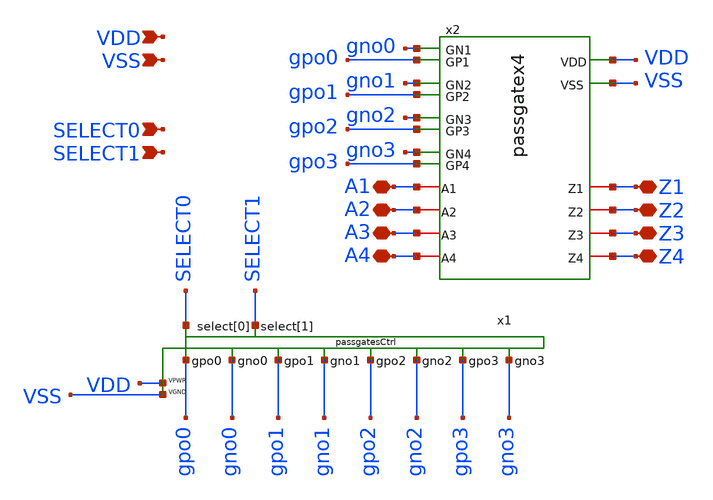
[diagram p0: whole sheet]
** sch_path: xschem/mux4onehot.sch
**.subckt mux4onehot VSS VDD A1 A2 A3 A4 Z1 Z2 Z3 Z4 SELECT0 SELECT1
*.ipin VSS
*.ipin VDD
*.iopin A1
*.iopin A2
*.iopin A3
*.iopin A4
*.iopin Z1
*.iopin Z2
*.iopin Z3
*.iopin Z4
*.ipin SELECT0
*.ipin SELECT1
x1 VSS VDD gno0 gno1 gno2 gno3 gpo0 gpo1 gpo2 gpo3 SELECT0 SELECT1 passgatesCtrl
x2 gpo2 gpo1 gpo0 VDD gpo3 VSS A3 A2 A1 Z3 Z1 Z2 A4 Z4 gno2 gno1 gno0 gno3 passgatex4
**.ends

* expanding   symbol:  /home/ttuser/vmswap/tt09-analogmux/xschem/passgatex4.sym # of pins=18
** sym_path: xschem/passgatex4.sym
** sch_path: xschem/passgatex4.sch
.subckt passgatex4 GP3 GP2 GP1 VDD GP4 VSS A3 A2 A1 Z3 Z1 Z2 A4 Z4 GN3 GN2 GN1 GN4
*.ipin VDD
*.ipin VSS
*.ipin GP1
*.ipin GN1
*.iopin A1
*.iopin Z1
*.ipin GP2
*.ipin GN2
*.iopin A2
*.iopin Z2
*.ipin GP3
*.ipin GN3
*.iopin A3
*.iopin Z3
*.ipin GP4
*.ipin GN4
*.iopin A4
*.iopin Z4
x1 Z1 A1 GP1 GN1 VSS VDD passgate
x2 Z2 A2 GP2 GN2 VSS VDD passgate
x3 Z3 A3 GP3 GN3 VSS VDD passgate
x4 Z4 A4 GP4 GN4 VSS VDD passgate
.ends


* expanding   symbol:  /home/ttuser/tt08-wowa2/xschem/passgate.sym # of pins=6
** sym_path: xschem/passgate.sym
** sch_path: xschem/passgate.sch
.subckt passgate Z A GP GN VSSBPIN VCCBPIN
*.ipin GN
*.ipin VCCBPIN
*.ipin VSSBPIN
*.ipin GP
*.iopin A
*.iopin Z
XM1 Z GN A VSSBPIN sky130_fd_pr__nfet_01v8_lvt L=0.35 W=8 nf=1 ad='int((nf+1)/2) * W/nf * 0.29' as='int((nf+2)/2) * W/nf * 0.29'
+ pd='2*int((nf+1)/2) * (W/nf + 0.29)' ps='2*int((nf+2)/2) * (W/nf + 0.29)' nrd='0.29 / W' nrs='0.29 / W'
+ sa=0 sb=0 sd=0 mult=2 m=2
XM3 Z GP A VCCBPIN sky130_fd_pr__pfet_01v8_lvt L=0.35 W=10 nf=1 ad='int((nf+1)/2) * W/nf * 0.29' as='int((nf+2)/2) * W/nf * 0.29'
+ pd='2*int((nf+1)/2) * (W/nf + 0.29)' ps='2*int((nf+2)/2) * (W/nf + 0.29)' nrd='0.29 / W' nrs='0.29 / W'
+ sa=0 sb=0 sd=0 mult=2 m=2
.ends

.end
